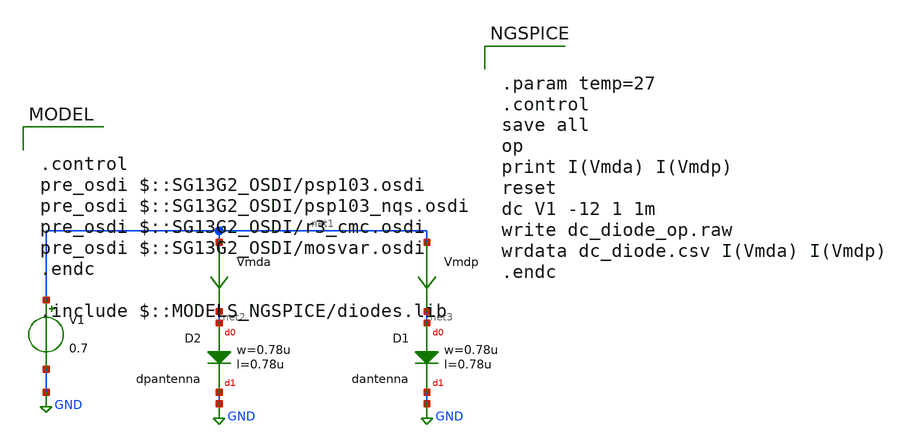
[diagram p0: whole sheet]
** sch_path: ihp-sg13g2/xschem_libs/sg13g2_tests/dc_diode_op/schematic/dc_diode_op.sch
* Copyright 2023 IHP PDK Authors
**.subckt dc_diode_op
V1 net1 GND 0.7
Vmda net1 net2 0
.save i(vmda)
Vmdp net1 net3 0
.save i(vmdp)
XD2 net2 GND dpantenna l=0.78u w=0.78u
XD1 net3 GND dantenna l=0.78u w=0.78u
**** begin user architecture code

.control
pre_osdi $::SG13G2_OSDI/psp103.osdi
pre_osdi $::SG13G2_OSDI/psp103_nqs.osdi
pre_osdi $::SG13G2_OSDI/r3_cmc.osdi
pre_osdi $::SG13G2_OSDI/mosvar.osdi
.endc

.include $::MODELS_NGSPICE/diodes.lib



.param temp=27
.control
save all
op
print I(Vmda) I(Vmdp)
reset
dc V1 -12 1 1m
write dc_diode_op.raw
wrdata dc_diode.csv I(Vmda) I(Vmdp)
.endc


**** end user architecture code
**.ends
.GLOBAL GND
.end
